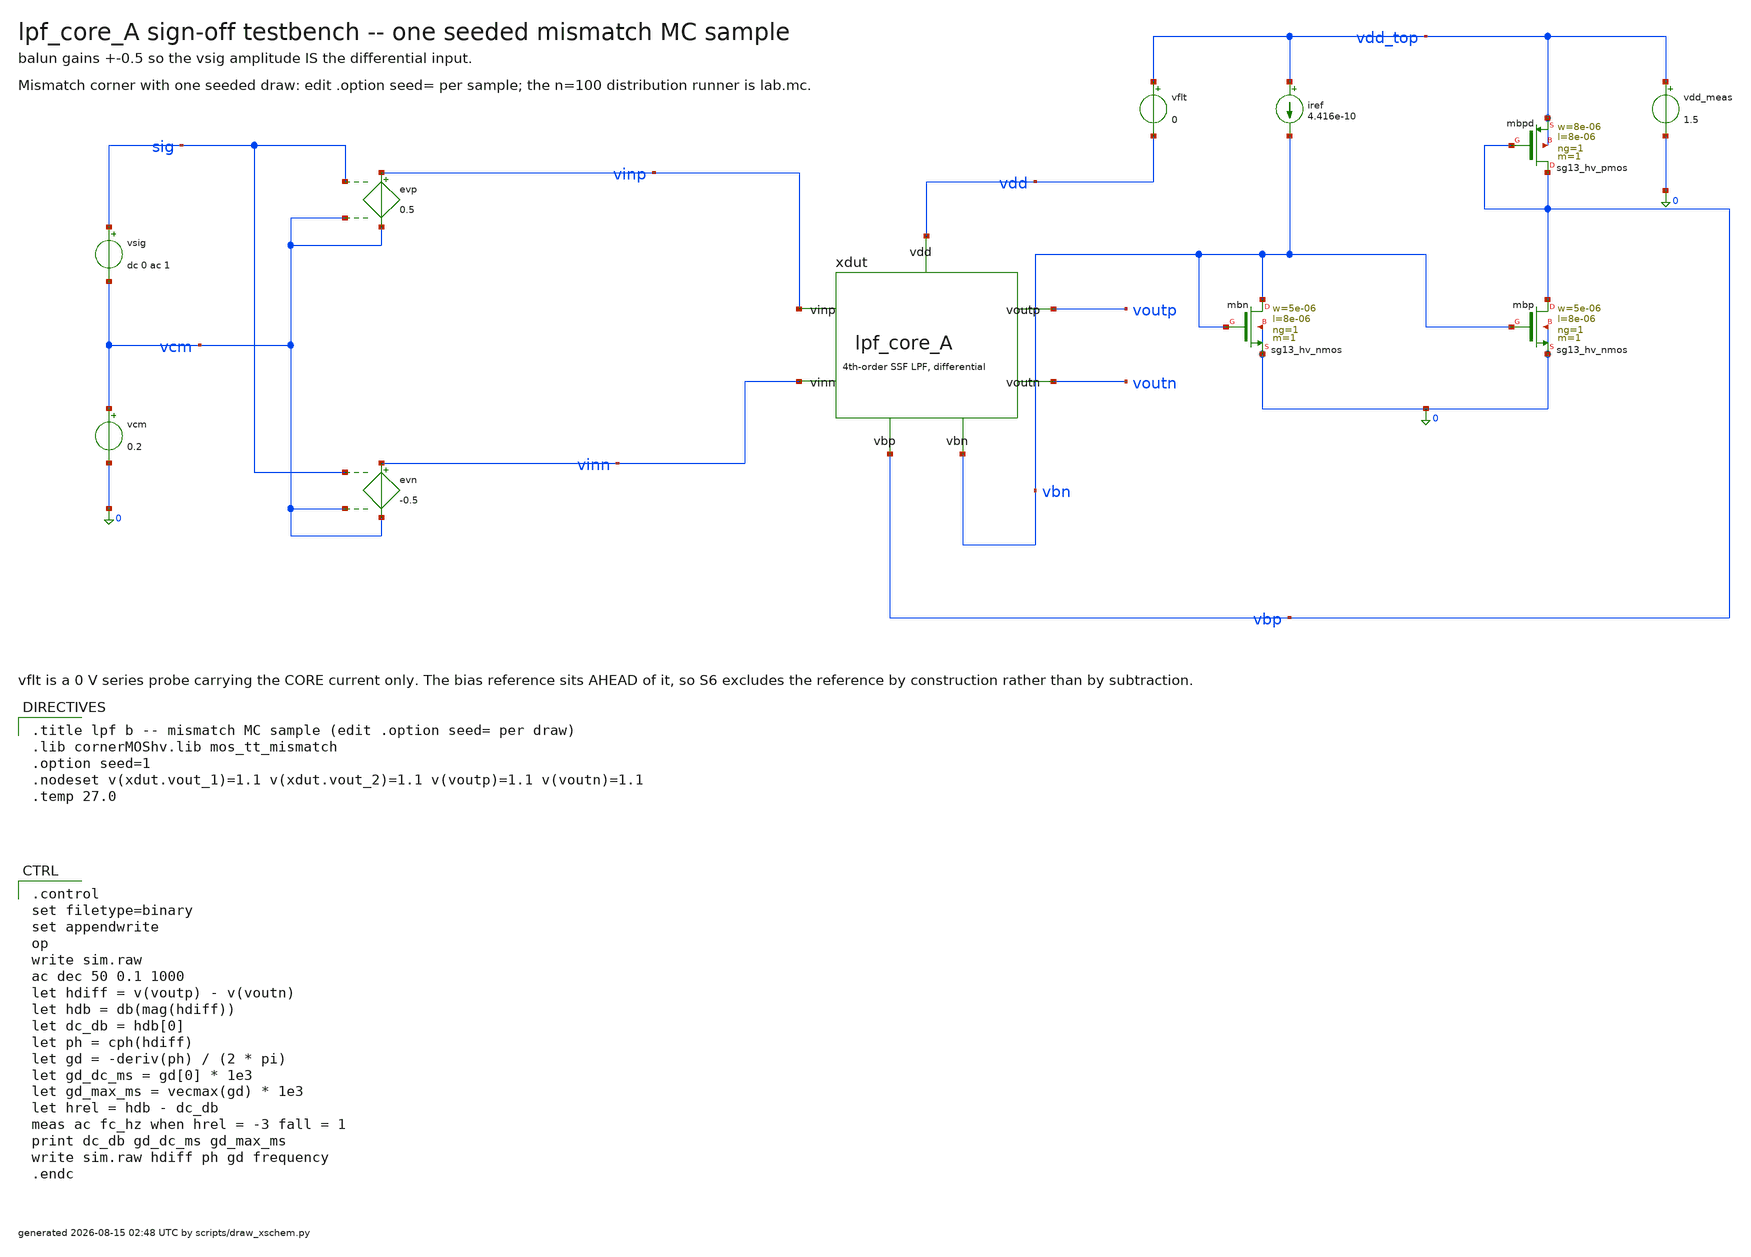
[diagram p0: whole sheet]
** sch_path: signoff/A-minarea/lpf_tb_A_mc.sch
**.subckt lpf_tb_A_mc
vsig sig vcm dc 0 ac 1
vcm vcm 0 0.2
evp vinp vcm sig vcm 0.5
evn vinn vcm sig vcm -0.5
xdut vinp vinn voutp voutn vbn vbp vdd lpf_core_A
vflt vdd_top vdd 0
vdd_meas vdd_top 0 1.5
iref vdd_top vbn 4.416e-10
Xmbn vbn vbn 0 0 sg13_hv_nmos w=5e-06 l=8e-06 ng=1 m=1 mm_ok=1
Xmbp vbp vbn 0 0 sg13_hv_nmos w=5e-06 l=8e-06 ng=1 m=1 mm_ok=1
Xmbpd vbp vbp vdd_top vdd_top sg13_hv_pmos w=8e-06 l=8e-06 ng=1 m=1 mm_ok=1
**** begin user architecture code

.title lpf b -- mismatch MC sample (edit .option seed= per draw)
.lib cornerMOShv.lib mos_tt_mismatch
.option seed=1
.nodeset v(xdut.vout_1)=1.1 v(xdut.vout_2)=1.1 v(voutp)=1.1 v(voutn)=1.1
.temp 27.0


.control
set filetype=binary
set appendwrite
op
write sim.raw
ac dec 50 0.1 1000
let hdiff = v(voutp) - v(voutn)
let hdb = db(mag(hdiff))
let dc_db = hdb[0]
let ph = cph(hdiff)
let gd = -deriv(ph) / (2 * pi)
let gd_dc_ms = gd[0] * 1e3
let gd_max_ms = vecmax(gd) * 1e3
let hrel = hdb - dc_db
meas ac fc_hz when hrel = -3 fall = 1
print dc_db gd_dc_ms gd_max_ms
write sim.raw hdiff ph gd frequency
.endc

**** end user architecture code
**.ends
.end
